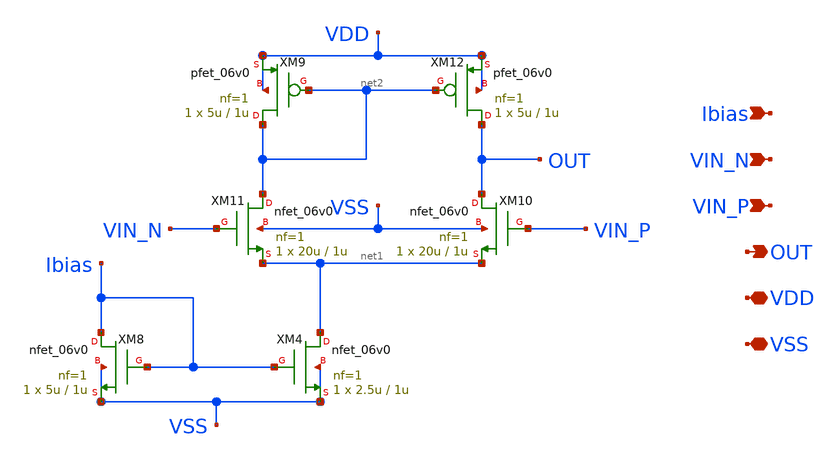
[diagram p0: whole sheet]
** sch_path: week02_current_diffpair/tugas5_cascode_current_mirror/5t-ota.sch
**.subckt 5t-ota VIN_N VIN_P OUT VDD VSS Ibias
*.ipin VIN_N
*.ipin VIN_P
*.opin OUT
*.iopin VDD
*.iopin VSS
*.ipin Ibias
XM4 net1 Ibias VSS VSS nfet_06v0 L=1u W=2.5u nf=1 ad='int((nf+1)/2) * W/nf * 0.18u' as='int((nf+2)/2) * W/nf * 0.18u'
+ pd='2*int((nf+1)/2) * (W/nf + 0.18u)' ps='2*int((nf+2)/2) * (W/nf + 0.18u)' nrd='0.18u / W' nrs='0.18u / W'
+ sa=0 sb=0 sd=0 m=1
XM8 Ibias Ibias VSS VSS nfet_06v0 L=1u W=5u nf=1 ad='int((nf+1)/2) * W/nf * 0.18u' as='int((nf+2)/2) * W/nf * 0.18u'
+ pd='2*int((nf+1)/2) * (W/nf + 0.18u)' ps='2*int((nf+2)/2) * (W/nf + 0.18u)' nrd='0.18u / W' nrs='0.18u / W'
+ sa=0 sb=0 sd=0 m=1
XM9 net2 net2 VDD VDD pfet_06v0 L=1u W=5u nf=1 ad='int((nf+1)/2) * W/nf * 0.18u' as='int((nf+2)/2) * W/nf * 0.18u'
+ pd='2*int((nf+1)/2) * (W/nf + 0.18u)' ps='2*int((nf+2)/2) * (W/nf + 0.18u)' nrd='0.18u / W' nrs='0.18u / W'
+ sa=0 sb=0 sd=0 m=1
XM10 OUT VIN_P net1 VSS nfet_06v0 L=1u W=20u nf=1 ad='int((nf+1)/2) * W/nf * 0.18u' as='int((nf+2)/2) * W/nf * 0.18u'
+ pd='2*int((nf+1)/2) * (W/nf + 0.18u)' ps='2*int((nf+2)/2) * (W/nf + 0.18u)' nrd='0.18u / W' nrs='0.18u / W'
+ sa=0 sb=0 sd=0 m=1
XM11 net2 VIN_N net1 VSS nfet_06v0 L=1u W=20u nf=1 ad='int((nf+1)/2) * W/nf * 0.18u' as='int((nf+2)/2) * W/nf * 0.18u'
+ pd='2*int((nf+1)/2) * (W/nf + 0.18u)' ps='2*int((nf+2)/2) * (W/nf + 0.18u)' nrd='0.18u / W' nrs='0.18u / W'
+ sa=0 sb=0 sd=0 m=1
XM12 OUT net2 VDD VDD pfet_06v0 L=1u W=5u nf=1 ad='int((nf+1)/2) * W/nf * 0.18u' as='int((nf+2)/2) * W/nf * 0.18u'
+ pd='2*int((nf+1)/2) * (W/nf + 0.18u)' ps='2*int((nf+2)/2) * (W/nf + 0.18u)' nrd='0.18u / W' nrs='0.18u / W'
+ sa=0 sb=0 sd=0 m=1
**.ends
.end
